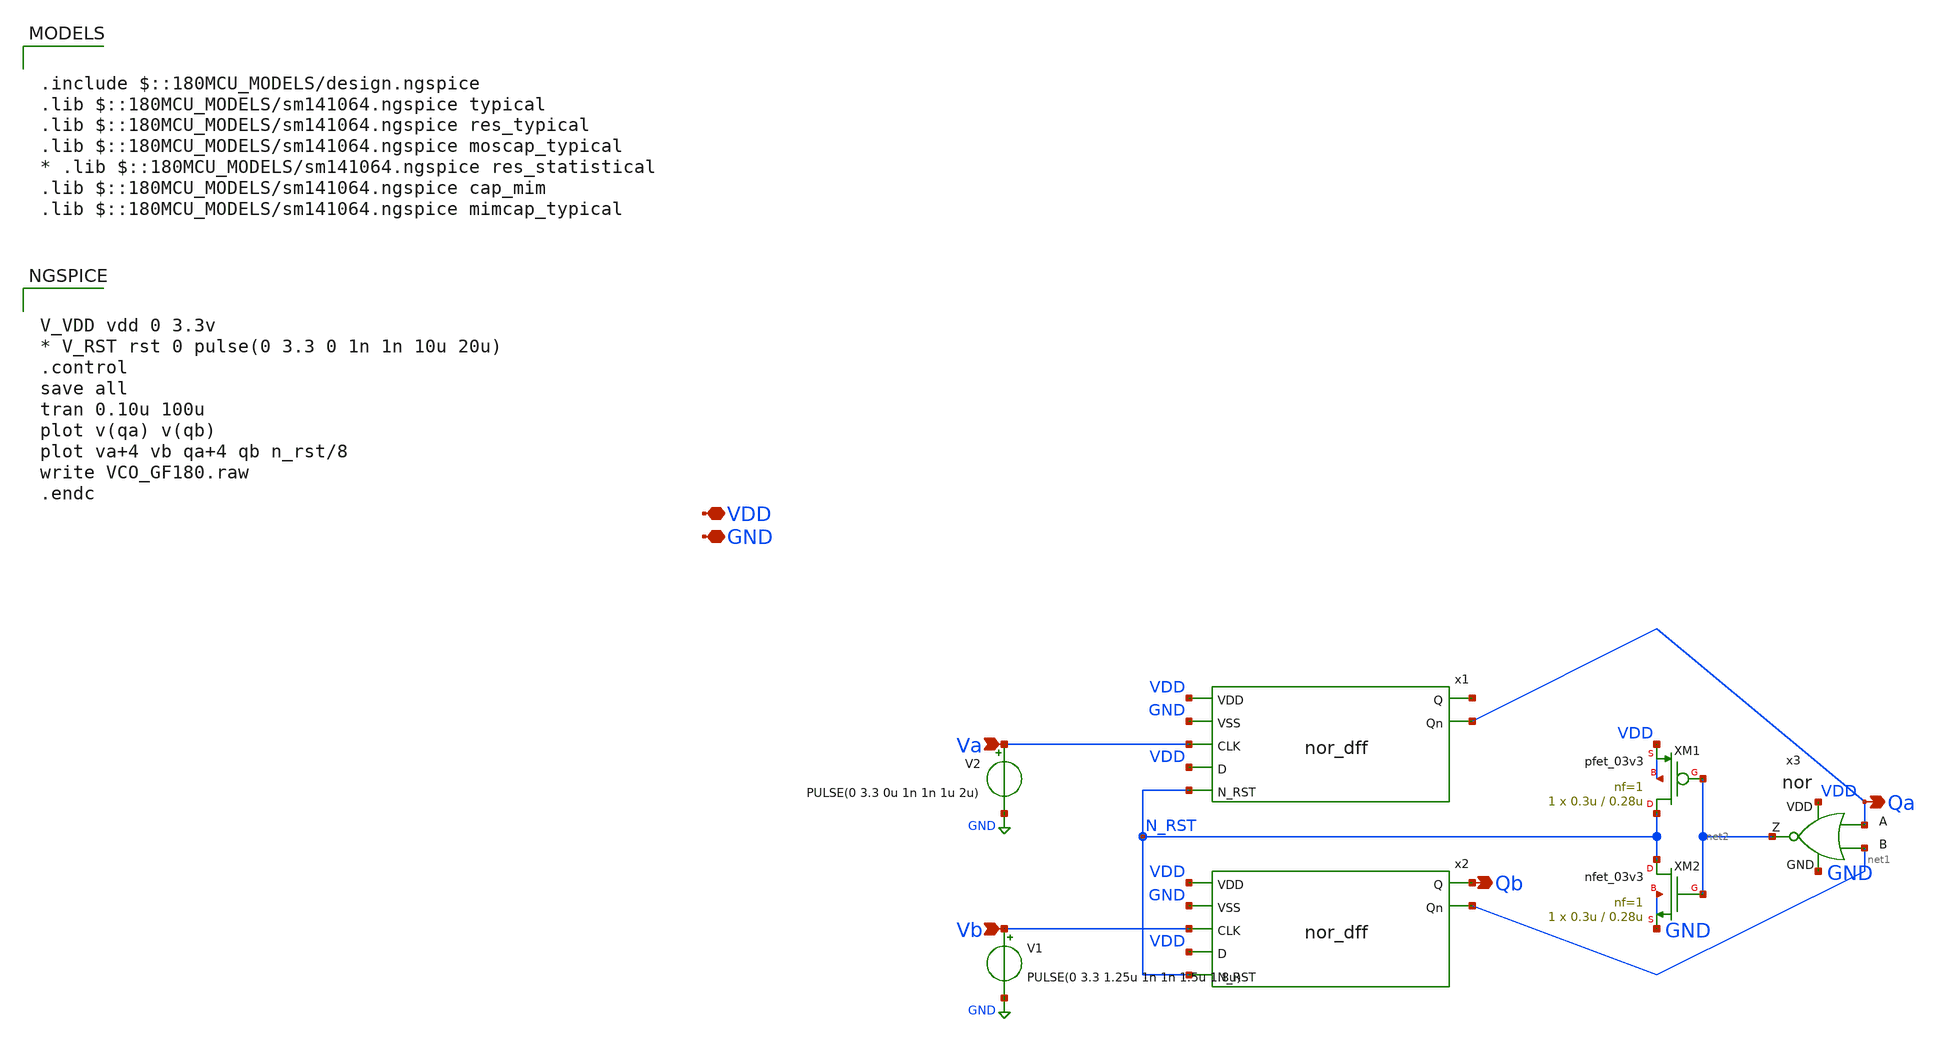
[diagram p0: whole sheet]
** sch_path: rha-vga-pll-blocks/blocks/pll/pfd.sch
**.subckt pfd Vb Va Qa Qb VDD GND
*.ipin Vb
*.ipin Va
*.opin Qa
*.opin Qb
*.iopin VDD
*.iopin GND
V2 Va GND PULSE(0 3.3 0u 1n 1n 1u 2u)
V1 Vb GND PULSE(0 3.3 1.25u 1n 1n 1.5u 1.8u)
x1 VDD GND Va VDD net3 N_RST Qa nor_dff
x2 VDD GND Vb VDD Qb N_RST net1 nor_dff
XM1 N_RST net2 VDD VDD pfet_03v3 L=0.28u W=0.3u nf=1 ad='int((nf+1)/2) * W/nf * 0.18u' as='int((nf+2)/2) * W/nf * 0.18u'
+ pd='2*int((nf+1)/2) * (W/nf + 0.18u)' ps='2*int((nf+2)/2) * (W/nf + 0.18u)' nrd='0.18u / W' nrs='0.18u / W'
+ sa=0 sb=0 sd=0 m=1
XM2 N_RST net2 GND GND nfet_03v3 L=0.28u W=0.3u nf=1 ad='int((nf+1)/2) * W/nf * 0.18u' as='int((nf+2)/2) * W/nf * 0.18u'
+ pd='2*int((nf+1)/2) * (W/nf + 0.18u)' ps='2*int((nf+2)/2) * (W/nf + 0.18u)' nrd='0.18u / W' nrs='0.18u / W'
+ sa=0 sb=0 sd=0 m=1
x3 VDD Qa net1 net2 GND nor
**** begin user architecture code

.include $::180MCU_MODELS/design.ngspice
.lib $::180MCU_MODELS/sm141064.ngspice typical
.lib $::180MCU_MODELS/sm141064.ngspice res_typical
.lib $::180MCU_MODELS/sm141064.ngspice moscap_typical
* .lib $::180MCU_MODELS/sm141064.ngspice res_statistical
.lib $::180MCU_MODELS/sm141064.ngspice cap_mim
.lib $::180MCU_MODELS/sm141064.ngspice mimcap_typical



V_VDD vdd 0 3.3v
* V_RST rst 0 pulse(0 3.3 0 1n 1n 10u 20u)
.control
save all
tran 0.10u 100u
plot v(qa) v(qb)
plot va+4 vb qa+4 qb n_rst/8
write VCO_GF180.raw
.endc


**** end user architecture code
**.ends
.GLOBAL GND
.end
